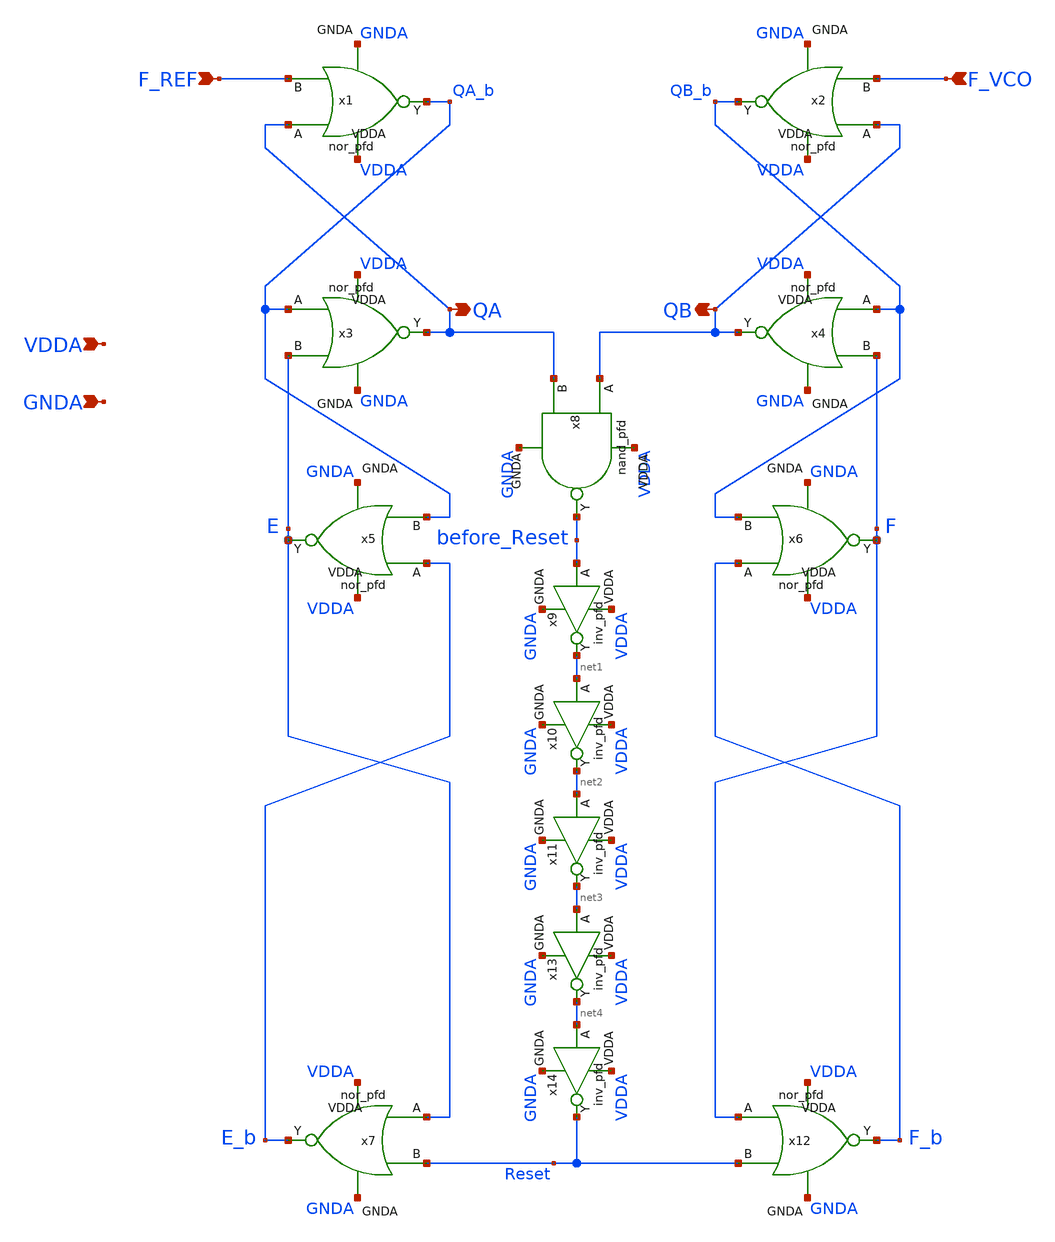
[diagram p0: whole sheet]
** sch_path: projects/pll/pfd/xschem_ngspice/phase_frequency_detector_5.sch
**.subckt phase_frequency_detector_5 F_REF QA F_VCO QB VDDA GNDA
*.ipin F_REF
*.opin QA
*.ipin F_VCO
*.opin QB
*.ipin VDDA
*.ipin GNDA
x1 VDDA GNDA QA F_REF QA_b nor_pfd
x2 VDDA GNDA QB F_VCO QB_b nor_pfd
x3 VDDA GNDA QA_b E QA nor_pfd
x4 VDDA GNDA QB_b F QB nor_pfd
x5 VDDA GNDA E_b QA_b E nor_pfd
x6 VDDA GNDA F_b QB_b F nor_pfd
x7 VDDA GNDA E Reset E_b nor_pfd
x12 VDDA GNDA F Reset F_b nor_pfd
x8 VDDA GNDA QB QA before_Reset nand_pfd
x9 VDDA GNDA before_Reset net1 inv_pfd
x10 VDDA GNDA net1 net2 inv_pfd
x11 VDDA GNDA net2 net3 inv_pfd
x13 VDDA GNDA net3 net4 inv_pfd
x14 VDDA GNDA net4 Reset inv_pfd
**.ends

* expanding   symbol:  /foss/designs/my_design/projects/pll/pfd/xschem_ngspice/nor_pfd.sym # of
*+ pins=5
** sym_path: projects/pll/pfd/xschem_ngspice/nor_pfd.sym
** sch_path: projects/pll/pfd/xschem_ngspice/nor_pfd.sch
.subckt nor_pfd VDDA GNDA A B Y
*.ipin A
*.opin Y
*.ipin VDDA
*.ipin GNDA
*.ipin B
XM4 net1 B VDDA VDDA sky130_fd_pr__pfet_01v8 L=0.15 W=2 nf=1 ad='int((nf+1)/2) * W/nf * 0.29' as='int((nf+2)/2) * W/nf * 0.29'
+ pd='2*int((nf+1)/2) * (W/nf + 0.29)' ps='2*int((nf+2)/2) * (W/nf + 0.29)' nrd='0.29 / W' nrs='0.29 / W'
+ sa=0 sb=0 sd=0 mult=1 m=1
XM2 GNDA B Y GNDA sky130_fd_pr__nfet_01v8 L=0.15 W=1 nf=1 ad='int((nf+1)/2) * W/nf * 0.29' as='int((nf+2)/2) * W/nf * 0.29'
+ pd='2*int((nf+1)/2) * (W/nf + 0.29)' ps='2*int((nf+2)/2) * (W/nf + 0.29)' nrd='0.29 / W' nrs='0.29 / W'
+ sa=0 sb=0 sd=0 mult=1 m=1
XM1 GNDA A Y GNDA sky130_fd_pr__nfet_01v8 L=0.15 W=1 nf=1 ad='int((nf+1)/2) * W/nf * 0.29' as='int((nf+2)/2) * W/nf * 0.29'
+ pd='2*int((nf+1)/2) * (W/nf + 0.29)' ps='2*int((nf+2)/2) * (W/nf + 0.29)' nrd='0.29 / W' nrs='0.29 / W'
+ sa=0 sb=0 sd=0 mult=1 m=1
XM3 Y A net1 VDDA sky130_fd_pr__pfet_01v8 L=0.15 W=2 nf=1 ad='int((nf+1)/2) * W/nf * 0.29' as='int((nf+2)/2) * W/nf * 0.29'
+ pd='2*int((nf+1)/2) * (W/nf + 0.29)' ps='2*int((nf+2)/2) * (W/nf + 0.29)' nrd='0.29 / W' nrs='0.29 / W'
+ sa=0 sb=0 sd=0 mult=1 m=1
.ends


* expanding   symbol:  /foss/designs/my_design/projects/pll/pfd/xschem_ngspice/nand_pfd.sym # of
*+ pins=5
** sym_path: projects/pll/pfd/xschem_ngspice/nand_pfd.sym
** sch_path: projects/pll/pfd/xschem_ngspice/nand_pfd.sch
.subckt nand_pfd VDDA GNDA A B Y
*.ipin A
*.opin Y
*.ipin VDDA
*.ipin GNDA
*.ipin B
XM4 Y B VDDA VDDA sky130_fd_pr__pfet_01v8 L=0.15 W=1 nf=2 ad='int((nf+1)/2) * W/nf * 0.29' as='int((nf+2)/2) * W/nf * 0.29'
+ pd='2*int((nf+1)/2) * (W/nf + 0.29)' ps='2*int((nf+2)/2) * (W/nf + 0.29)' nrd='0.29 / W' nrs='0.29 / W'
+ sa=0 sb=0 sd=0 mult=1 m=1
XM2 net1 B Y GNDA sky130_fd_pr__nfet_01v8 L=0.15 W=0.5 nf=1 ad='int((nf+1)/2) * W/nf * 0.29' as='int((nf+2)/2) * W/nf * 0.29'
+ pd='2*int((nf+1)/2) * (W/nf + 0.29)' ps='2*int((nf+2)/2) * (W/nf + 0.29)' nrd='0.29 / W' nrs='0.29 / W'
+ sa=0 sb=0 sd=0 mult=1 m=1
XM1 GNDA A net1 GNDA sky130_fd_pr__nfet_01v8 L=0.15 W=0.5 nf=1 ad='int((nf+1)/2) * W/nf * 0.29' as='int((nf+2)/2) * W/nf * 0.29'
+ pd='2*int((nf+1)/2) * (W/nf + 0.29)' ps='2*int((nf+2)/2) * (W/nf + 0.29)' nrd='0.29 / W' nrs='0.29 / W'
+ sa=0 sb=0 sd=0 mult=1 m=1
XM3 Y A VDDA VDDA sky130_fd_pr__pfet_01v8 L=0.15 W=1 nf=2 ad='int((nf+1)/2) * W/nf * 0.29' as='int((nf+2)/2) * W/nf * 0.29'
+ pd='2*int((nf+1)/2) * (W/nf + 0.29)' ps='2*int((nf+2)/2) * (W/nf + 0.29)' nrd='0.29 / W' nrs='0.29 / W'
+ sa=0 sb=0 sd=0 mult=1 m=1
.ends


* expanding   symbol:  /foss/designs/my_design/projects/pll/pfd/xschem_ngspice/inv_pfd.sym # of
*+ pins=4
** sym_path: projects/ASU/EEE572/schematic/inv_pfd.sym
** sch_path: projects/ASU/EEE572/schematic/inv_pfd.sch
.subckt inv_pfd VDDA GNDA A Y
*.ipin A
*.opin Y
*.ipin VDDA
*.ipin GNDA
XM2 Y A VDDA VDDA sky130_fd_pr__pfet_01v8 L=0.15 W=2 nf=1 ad='int((nf+1)/2) * W/nf * 0.29' as='int((nf+2)/2) * W/nf * 0.29'
+ pd='2*int((nf+1)/2) * (W/nf + 0.29)' ps='2*int((nf+2)/2) * (W/nf + 0.29)' nrd='0.29 / W' nrs='0.29 / W'
+ sa=0 sb=0 sd=0 mult=1 m=1
XM1 GNDA A Y GNDA sky130_fd_pr__nfet_01v8 L=0.15 W=1 nf=1 ad='int((nf+1)/2) * W/nf * 0.29' as='int((nf+2)/2) * W/nf * 0.29'
+ pd='2*int((nf+1)/2) * (W/nf + 0.29)' ps='2*int((nf+2)/2) * (W/nf + 0.29)' nrd='0.29 / W' nrs='0.29 / W'
+ sa=0 sb=0 sd=0 mult=1 m=1
.ends

.end
